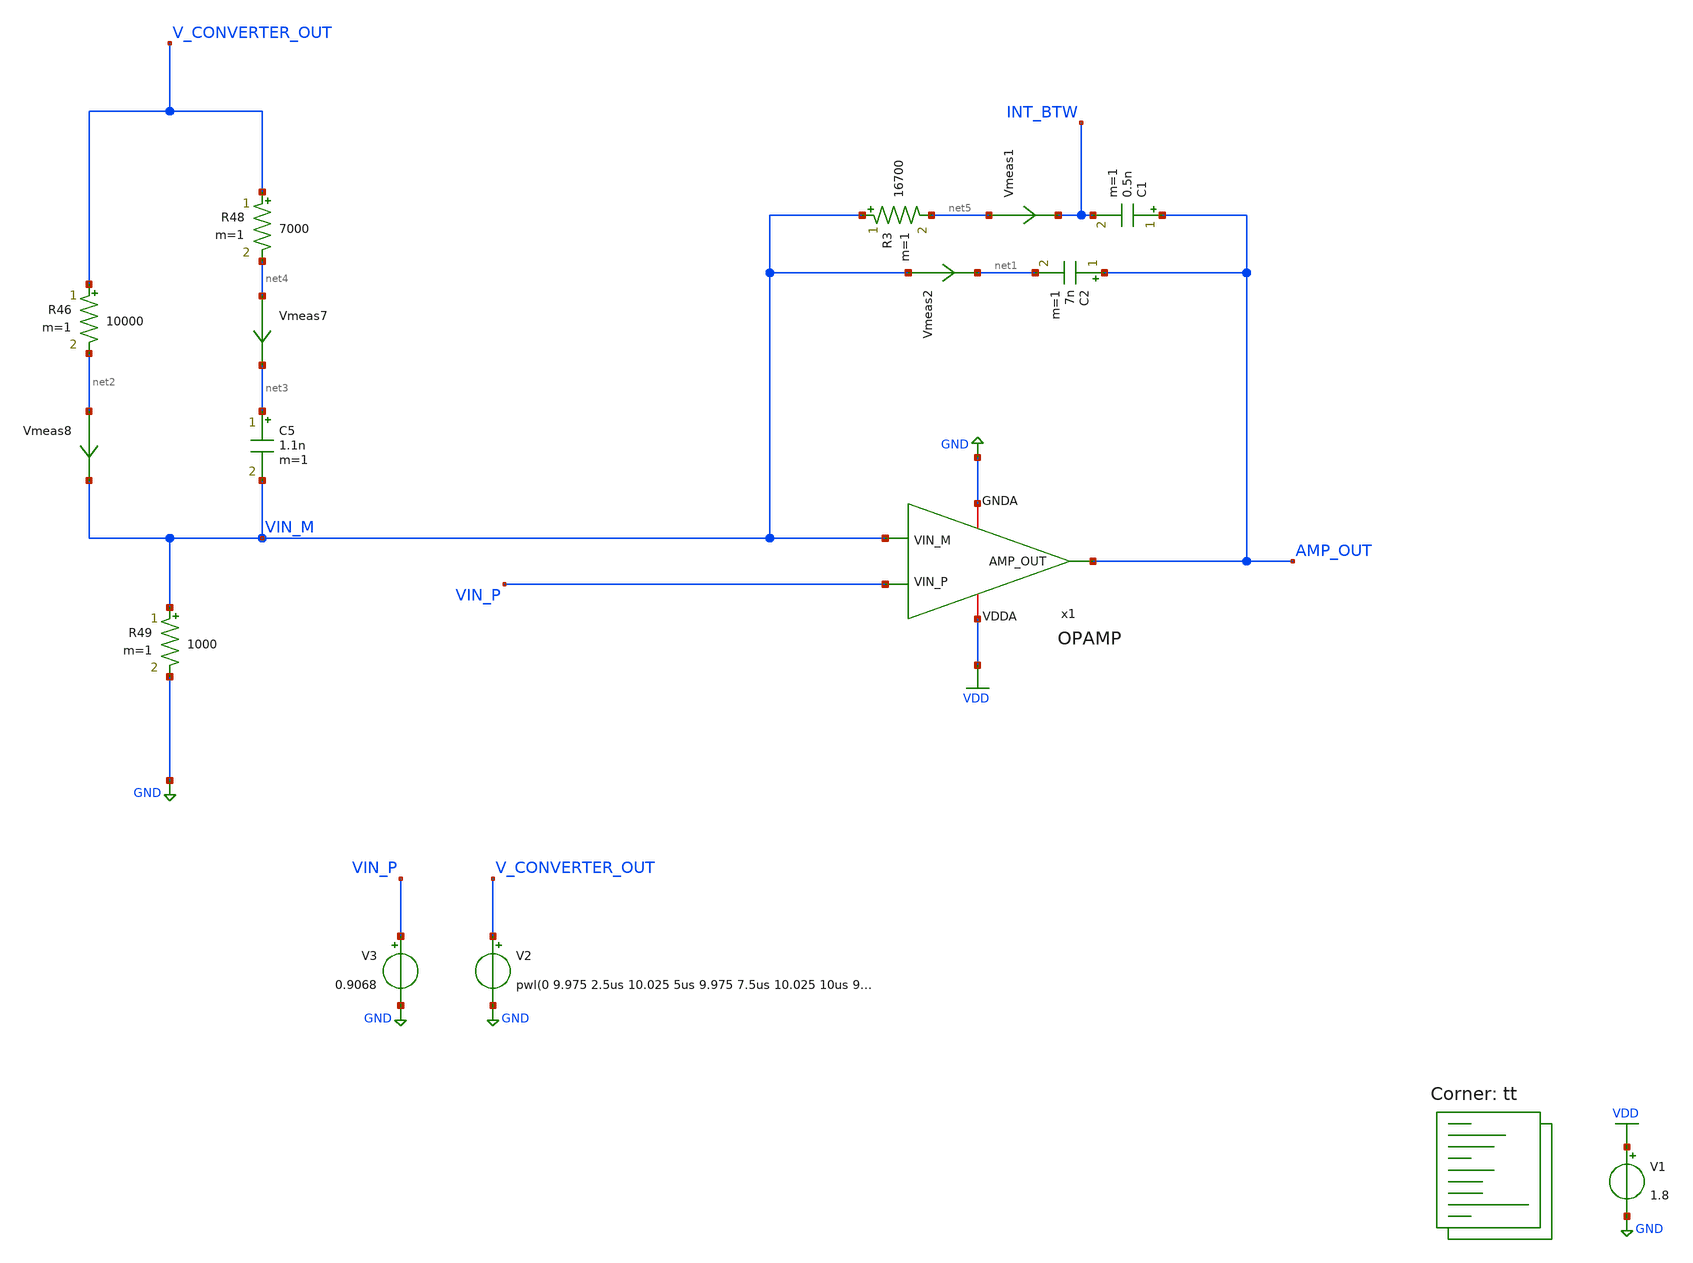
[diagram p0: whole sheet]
** sch_path: projects/ASU/EEE572/schematic/tb_integrator.sch
**.subckt tb_integrator
V1 VDD GND 1.8
V2 V_CONVERTER_OUT GND pwl(0 9.975 2.5us 10.025 5us 9.975 7.5us 10.025 10us 9.975 12.5us 10.025 15us
+ 9.975 17.5us 10.025 20us 9.975 22.5us 10.025 25us 9.975)
x1 VDD AMP_OUT VIN_P VIN_M GND OPAMP
V3 VIN_P GND 0.9068
C1 AMP_OUT INT_BTW 0.5n m=1
C2 AMP_OUT net1 7n m=1
Vmeas1 net5 INT_BTW 0
.save i(vmeas1)
Vmeas2 VIN_M net1 0
.save i(vmeas2)
R46 V_CONVERTER_OUT net2 10000 m=1
R48 V_CONVERTER_OUT net4 7000 m=1
C5 net3 VIN_M 1.1n m=1
R49 VIN_M GND 1000 m=1
Vmeas7 net4 net3 0
.save i(vmeas7)
Vmeas8 net2 VIN_M 0
.save i(vmeas8)
R3 VIN_M net5 16700 m=1
**** begin user architecture code
.lib $::SKYWATER_MODELS/sky130.lib.spice tt



.options method=gear
.options wnflag=1
* .options savecurrents

.control

  save v(vin_p) v(vin_m) v(vin_m2) v(int_btw) v(v_converter_out) v(amp_out) v(ph(amp_out))
  * save all
  * tran 0.1ns 4us
  * tran 0.01ns 0.4us
  tran 0.5ns 25us
  remzerovec
  write tb_integrator.raw
  set appendwrite

.endc




**** end user architecture code
**.ends

* expanding   symbol:  OPAMP.sym # of pins=5
** sym_path: projects/ASU/EEE572/schematic/OPAMP.sym
** sch_path: projects/ASU/EEE572/schematic/OPAMP.sch
.subckt OPAMP VDDA AMP_OUT VIN_P VIN_M GNDA
*.iopin GNDA
*.iopin VDDA
*.ipin VIN_P
*.ipin VIN_M
*.opin AMP_OUT
XM1 V_REF V_REF V_RES GNDA sky130_fd_pr__nfet_01v8 L=0.3 W=16 nf=8 ad='int((nf+1)/2) * W/nf * 0.29' as='int((nf+2)/2) * W/nf * 0.29'
+ pd='2*int((nf+1)/2) * (W/nf + 0.29)' ps='2*int((nf+2)/2) * (W/nf + 0.29)' nrd='0.29 / W' nrs='0.29 / W'
+ sa=0 sb=0 sd=0 mult=1 m=1
XM2 V_REF_MIR V_REF_MIR GNDA GNDA sky130_fd_pr__nfet_01v8 L=0.3 W=4 nf=2 ad='int((nf+1)/2) * W/nf * 0.29'
+ as='int((nf+2)/2) * W/nf * 0.29' pd='2*int((nf+1)/2) * (W/nf + 0.29)' ps='2*int((nf+2)/2) * (W/nf + 0.29)'
+ nrd='0.29 / W' nrs='0.29 / W' sa=0 sb=0 sd=0 mult=1 m=1
XM5 START_UP V_REF_MIR GNDA GNDA sky130_fd_pr__nfet_01v8 L=0.3 W=4 nf=2 ad='int((nf+1)/2) * W/nf * 0.29'
+ as='int((nf+2)/2) * W/nf * 0.29' pd='2*int((nf+1)/2) * (W/nf + 0.29)' ps='2*int((nf+2)/2) * (W/nf + 0.29)'
+ nrd='0.29 / W' nrs='0.29 / W' sa=0 sb=0 sd=0 mult=1 m=1
XM7 Vbiasp START_UP V_REF_MIR GNDA sky130_fd_pr__nfet_01v8 L=0.3 W=4 nf=2 ad='int((nf+1)/2) * W/nf * 0.29'
+ as='int((nf+2)/2) * W/nf * 0.29' pd='2*int((nf+1)/2) * (W/nf + 0.29)' ps='2*int((nf+2)/2) * (W/nf + 0.29)'
+ nrd='0.29 / W' nrs='0.29 / W' sa=0 sb=0 sd=0 mult=1 m=1
XM6 START_UP START_UP VDD VDD sky130_fd_pr__pfet_01v8 L=20 W=0.5 nf=1 ad='int((nf+1)/2) * W/nf * 0.29'
+ as='int((nf+2)/2) * W/nf * 0.29' pd='2*int((nf+1)/2) * (W/nf + 0.29)' ps='2*int((nf+2)/2) * (W/nf + 0.29)'
+ nrd='0.29 / W' nrs='0.29 / W' sa=0 sb=0 sd=0 mult=1 m=1
XM3 V_REF Vbiasp VDDA VDDA sky130_fd_pr__pfet_01v8 L=0.3 W=12 nf=6 ad='int((nf+1)/2) * W/nf * 0.29' as='int((nf+2)/2) * W/nf * 0.29'
+ pd='2*int((nf+1)/2) * (W/nf + 0.29)' ps='2*int((nf+2)/2) * (W/nf + 0.29)' nrd='0.29 / W' nrs='0.29 / W'
+ sa=0 sb=0 sd=0 mult=1 m=1
XM4 V_REF_MIR Vbiasp VDDA VDDA sky130_fd_pr__pfet_01v8 L=0.3 W=12 nf=6 ad='int((nf+1)/2) * W/nf * 0.29'
+ as='int((nf+2)/2) * W/nf * 0.29' pd='2*int((nf+1)/2) * (W/nf + 0.29)' ps='2*int((nf+2)/2) * (W/nf + 0.29)'
+ nrd='0.29 / W' nrs='0.29 / W' sa=0 sb=0 sd=0 mult=1 m=1
XM8 Vbiasp V_REF_MIR GNDA GNDA sky130_fd_pr__nfet_01v8 L=0.3 W=4 nf=2 ad='int((nf+1)/2) * W/nf * 0.29'
+ as='int((nf+2)/2) * W/nf * 0.29' pd='2*int((nf+1)/2) * (W/nf + 0.29)' ps='2*int((nf+2)/2) * (W/nf + 0.29)'
+ nrd='0.29 / W' nrs='0.29 / W' sa=0 sb=0 sd=0 mult=1 m=1
XM9 Vbiasp_MIR V_REF GNDA GNDA sky130_fd_pr__nfet_01v8 L=0.3 W=4 nf=2 ad='int((nf+1)/2) * W/nf * 0.29'
+ as='int((nf+2)/2) * W/nf * 0.29' pd='2*int((nf+1)/2) * (W/nf + 0.29)' ps='2*int((nf+2)/2) * (W/nf + 0.29)'
+ nrd='0.29 / W' nrs='0.29 / W' sa=0 sb=0 sd=0 mult=1 m=1
XM10 Vbiasp Vbiasp_MIR VDDA VDDA sky130_fd_pr__pfet_01v8 L=0.3 W=12 nf=6 ad='int((nf+1)/2) * W/nf * 0.29'
+ as='int((nf+2)/2) * W/nf * 0.29' pd='2*int((nf+1)/2) * (W/nf + 0.29)' ps='2*int((nf+2)/2) * (W/nf + 0.29)'
+ nrd='0.29 / W' nrs='0.29 / W' sa=0 sb=0 sd=0 mult=1 m=1
XM11 Vbiasp_MIR Vbiasp_MIR VDDA VDDA sky130_fd_pr__pfet_01v8 L=0.3 W=12 nf=6 ad='int((nf+1)/2) * W/nf * 0.29'
+ as='int((nf+2)/2) * W/nf * 0.29' pd='2*int((nf+1)/2) * (W/nf + 0.29)' ps='2*int((nf+2)/2) * (W/nf + 0.29)'
+ nrd='0.29 / W' nrs='0.29 / W' sa=0 sb=0 sd=0 mult=1 m=1
XM12 Vbias3 Vbias3 GNDA GNDA sky130_fd_pr__nfet_01v8 L=4 W=4 nf=1 ad='int((nf+1)/2) * W/nf * 0.29' as='int((nf+2)/2) * W/nf * 0.29'
+ pd='2*int((nf+1)/2) * (W/nf + 0.29)' ps='2*int((nf+2)/2) * (W/nf + 0.29)' nrd='0.29 / W' nrs='0.29 / W'
+ sa=0 sb=0 sd=0 mult=1 m=1
XM13 Vbias3 Vbiasp VDDA VDDA sky130_fd_pr__pfet_01v8 L=0.3 W=12 nf=6 ad='int((nf+1)/2) * W/nf * 0.29'
+ as='int((nf+2)/2) * W/nf * 0.29' pd='2*int((nf+1)/2) * (W/nf + 0.29)' ps='2*int((nf+2)/2) * (W/nf + 0.29)'
+ nrd='0.29 / W' nrs='0.29 / W' sa=0 sb=0 sd=0 mult=1 m=1
XM14 net1 Vbias1 VDDA VDDA sky130_fd_pr__pfet_01v8 L=0.3 W=12 nf=6 ad='int((nf+1)/2) * W/nf * 0.29' as='int((nf+2)/2) * W/nf * 0.29'
+ pd='2*int((nf+1)/2) * (W/nf + 0.29)' ps='2*int((nf+2)/2) * (W/nf + 0.29)' nrd='0.29 / W' nrs='0.29 / W'
+ sa=0 sb=0 sd=0 mult=1 m=1
XM15 Vhigh Vbias1 VDDA VDDA sky130_fd_pr__pfet_01v8 L=0.3 W=12 nf=6 ad='int((nf+1)/2) * W/nf * 0.29'
+ as='int((nf+2)/2) * W/nf * 0.29' pd='2*int((nf+1)/2) * (W/nf + 0.29)' ps='2*int((nf+2)/2) * (W/nf + 0.29)'
+ nrd='0.29 / W' nrs='0.29 / W' sa=0 sb=0 sd=0 mult=1 m=1
XM16 Vncas Vbias2 net1 VDDA sky130_fd_pr__pfet_01v8 L=0.3 W=12 nf=6 ad='int((nf+1)/2) * W/nf * 0.29'
+ as='int((nf+2)/2) * W/nf * 0.29' pd='2*int((nf+1)/2) * (W/nf + 0.29)' ps='2*int((nf+2)/2) * (W/nf + 0.29)'
+ nrd='0.29 / W' nrs='0.29 / W' sa=0 sb=0 sd=0 mult=1 m=1
XM17 Vbias1 Vbias2 Vhigh VDDA sky130_fd_pr__pfet_01v8 L=0.3 W=12 nf=6 ad='int((nf+1)/2) * W/nf * 0.29'
+ as='int((nf+2)/2) * W/nf * 0.29' pd='2*int((nf+1)/2) * (W/nf + 0.29)' ps='2*int((nf+2)/2) * (W/nf + 0.29)'
+ nrd='0.29 / W' nrs='0.29 / W' sa=0 sb=0 sd=0 mult=1 m=1
XM18 net2 Vbias4 GNDA GNDA sky130_fd_pr__nfet_01v8 L=0.3 W=4 nf=2 ad='int((nf+1)/2) * W/nf * 0.29' as='int((nf+2)/2) * W/nf * 0.29'
+ pd='2*int((nf+1)/2) * (W/nf + 0.29)' ps='2*int((nf+2)/2) * (W/nf + 0.29)' nrd='0.29 / W' nrs='0.29 / W'
+ sa=0 sb=0 sd=0 mult=1 m=1
XM19 Vncas Vncas Vncas_btw GNDA sky130_fd_pr__nfet_01v8 L=0.3 W=4 nf=2 ad='int((nf+1)/2) * W/nf * 0.29'
+ as='int((nf+2)/2) * W/nf * 0.29' pd='2*int((nf+1)/2) * (W/nf + 0.29)' ps='2*int((nf+2)/2) * (W/nf + 0.29)'
+ nrd='0.29 / W' nrs='0.29 / W' sa=0 sb=0 sd=0 mult=1 m=1
XM20 Vncas_btw Vbias3 net3 GNDA sky130_fd_pr__nfet_01v8 L=0.3 W=4 nf=2 ad='int((nf+1)/2) * W/nf * 0.29'
+ as='int((nf+2)/2) * W/nf * 0.29' pd='2*int((nf+1)/2) * (W/nf + 0.29)' ps='2*int((nf+2)/2) * (W/nf + 0.29)'
+ nrd='0.29 / W' nrs='0.29 / W' sa=0 sb=0 sd=0 mult=1 m=1
XM21 net3 Vncas_btw GNDA GNDA sky130_fd_pr__nfet_01v8 L=0.3 W=4 nf=2 ad='int((nf+1)/2) * W/nf * 0.29'
+ as='int((nf+2)/2) * W/nf * 0.29' pd='2*int((nf+1)/2) * (W/nf + 0.29)' ps='2*int((nf+2)/2) * (W/nf + 0.29)'
+ nrd='0.29 / W' nrs='0.29 / W' sa=0 sb=0 sd=0 mult=1 m=1
XM25 Vbias4 Vbiasp VDDA VDDA sky130_fd_pr__pfet_01v8 L=0.3 W=12 nf=6 ad='int((nf+1)/2) * W/nf * 0.29'
+ as='int((nf+2)/2) * W/nf * 0.29' pd='2*int((nf+1)/2) * (W/nf + 0.29)' ps='2*int((nf+2)/2) * (W/nf + 0.29)'
+ nrd='0.29 / W' nrs='0.29 / W' sa=0 sb=0 sd=0 mult=1 m=1
XM27 Vbias4 Vbias3 Vlow GNDA sky130_fd_pr__nfet_01v8 L=0.3 W=4 nf=2 ad='int((nf+1)/2) * W/nf * 0.29'
+ as='int((nf+2)/2) * W/nf * 0.29' pd='2*int((nf+1)/2) * (W/nf + 0.29)' ps='2*int((nf+2)/2) * (W/nf + 0.29)'
+ nrd='0.29 / W' nrs='0.29 / W' sa=0 sb=0 sd=0 mult=1 m=1
XM28 Vlow Vbias4 GNDA GNDA sky130_fd_pr__nfet_01v8 L=0.3 W=4 nf=2 ad='int((nf+1)/2) * W/nf * 0.29' as='int((nf+2)/2) * W/nf * 0.29'
+ pd='2*int((nf+1)/2) * (W/nf + 0.29)' ps='2*int((nf+2)/2) * (W/nf + 0.29)' nrd='0.29 / W' nrs='0.29 / W'
+ sa=0 sb=0 sd=0 mult=1 m=1
XM29 Vds2 Vgs2 VDDA VDDA sky130_fd_pr__pfet_01v8 L=0.15 W=12 nf=6 ad='int((nf+1)/2) * W/nf * 0.29' as='int((nf+2)/2) * W/nf * 0.29'
+ pd='2*int((nf+1)/2) * (W/nf + 0.29)' ps='2*int((nf+2)/2) * (W/nf + 0.29)' nrd='0.29 / W' nrs='0.29 / W'
+ sa=0 sb=0 sd=0 mult=1 m=1
XM30 Vgs2 Vbias2 Vds2 VDDA sky130_fd_pr__pfet_01v8 L=0.15 W=12 nf=6 ad='int((nf+1)/2) * W/nf * 0.29'
+ as='int((nf+2)/2) * W/nf * 0.29' pd='2*int((nf+1)/2) * (W/nf + 0.29)' ps='2*int((nf+2)/2) * (W/nf + 0.29)'
+ nrd='0.29 / W' nrs='0.29 / W' sa=0 sb=0 sd=0 mult=1 m=1
XM31 Vpcas Vbias3 Vds3 GNDA sky130_fd_pr__nfet_01v8 L=0.3 W=4 nf=2 ad='int((nf+1)/2) * W/nf * 0.29' as='int((nf+2)/2) * W/nf * 0.29'
+ pd='2*int((nf+1)/2) * (W/nf + 0.29)' ps='2*int((nf+2)/2) * (W/nf + 0.29)' nrd='0.29 / W' nrs='0.29 / W'
+ sa=0 sb=0 sd=0 mult=1 m=1
XM32 Vds3 Vbias4 GNDA GNDA sky130_fd_pr__nfet_01v8 L=0.3 W=4 nf=2 ad='int((nf+1)/2) * W/nf * 0.29' as='int((nf+2)/2) * W/nf * 0.29'
+ pd='2*int((nf+1)/2) * (W/nf + 0.29)' ps='2*int((nf+2)/2) * (W/nf + 0.29)' nrd='0.29 / W' nrs='0.29 / W'
+ sa=0 sb=0 sd=0 mult=1 m=1
XM33 Vpcas Vpcas Vgs2 VDDA sky130_fd_pr__pfet_01v8 L=0.15 W=12 nf=1 ad='int((nf+1)/2) * W/nf * 0.29'
+ as='int((nf+2)/2) * W/nf * 0.29' pd='2*int((nf+1)/2) * (W/nf + 0.29)' ps='2*int((nf+2)/2) * (W/nf + 0.29)'
+ nrd='0.29 / W' nrs='0.29 / W' sa=0 sb=0 sd=0 mult=1 m=1
XM22 Vbias1 Vbias3 net2 GNDA sky130_fd_pr__nfet_01v8 L=0.3 W=4 nf=2 ad='int((nf+1)/2) * W/nf * 0.29'
+ as='int((nf+2)/2) * W/nf * 0.29' pd='2*int((nf+1)/2) * (W/nf + 0.29)' ps='2*int((nf+2)/2) * (W/nf + 0.29)'
+ nrd='0.29 / W' nrs='0.29 / W' sa=0 sb=0 sd=0 mult=1 m=1
XM23 Vbias2 Vbias2 VDDA VDDA sky130_fd_pr__pfet_01v8 L=1.5 W=12 nf=1 ad='int((nf+1)/2) * W/nf * 0.29'
+ as='int((nf+2)/2) * W/nf * 0.29' pd='2*int((nf+1)/2) * (W/nf + 0.29)' ps='2*int((nf+2)/2) * (W/nf + 0.29)'
+ nrd='0.29 / W' nrs='0.29 / W' sa=0 sb=0 sd=0 mult=1 m=1
XM24 net4 Vbias4 GNDA GNDA sky130_fd_pr__nfet_01v8 L=0.3 W=4 nf=2 ad='int((nf+1)/2) * W/nf * 0.29' as='int((nf+2)/2) * W/nf * 0.29'
+ pd='2*int((nf+1)/2) * (W/nf + 0.29)' ps='2*int((nf+2)/2) * (W/nf + 0.29)' nrd='0.29 / W' nrs='0.29 / W'
+ sa=0 sb=0 sd=0 mult=1 m=1
XM26 Vbias2 Vbias3 net4 GNDA sky130_fd_pr__nfet_01v8 L=0.3 W=4 nf=2 ad='int((nf+1)/2) * W/nf * 0.29'
+ as='int((nf+2)/2) * W/nf * 0.29' pd='2*int((nf+1)/2) * (W/nf + 0.29)' ps='2*int((nf+2)/2) * (W/nf + 0.29)'
+ nrd='0.29 / W' nrs='0.29 / W' sa=0 sb=0 sd=0 mult=1 m=1
XC1 Vbiasp VDDA sky130_fd_pr__cap_mim_m3_1 W=2 L=2 MF=4 m=4
XR1 GNDA V_RES GNDA sky130_fd_pr__res_high_po_0p35 L=10 mult=1 m=1
XM34 V_tail_btw Vbias4 GNDA GNDA sky130_fd_pr__nfet_01v8 L=0.3 W=12 nf=4 ad='int((nf+1)/2) * W/nf * 0.29'
+ as='int((nf+2)/2) * W/nf * 0.29' pd='2*int((nf+1)/2) * (W/nf + 0.29)' ps='2*int((nf+2)/2) * (W/nf + 0.29)'
+ nrd='0.29 / W' nrs='0.29 / W' sa=0 sb=0 sd=0 mult=3 m=3
XM35 Vp Vbias3 V_tail_btw GNDA sky130_fd_pr__nfet_01v8 L=0.3 W=12 nf=4 ad='int((nf+1)/2) * W/nf * 0.29'
+ as='int((nf+2)/2) * W/nf * 0.29' pd='2*int((nf+1)/2) * (W/nf + 0.29)' ps='2*int((nf+2)/2) * (W/nf + 0.29)'
+ nrd='0.29 / W' nrs='0.29 / W' sa=0 sb=0 sd=0 mult=3 m=3
XM36 Vd1 VIN_P Vp GNDA sky130_fd_pr__nfet_01v8 L=0.3 W=12 nf=4 ad='int((nf+1)/2) * W/nf * 0.29' as='int((nf+2)/2) * W/nf * 0.29'
+ pd='2*int((nf+1)/2) * (W/nf + 0.29)' ps='2*int((nf+2)/2) * (W/nf + 0.29)' nrd='0.29 / W' nrs='0.29 / W'
+ sa=0 sb=0 sd=0 mult=2 m=2
XM37 Vd2 VIN_M Vp GNDA sky130_fd_pr__nfet_01v8 L=0.3 W=12 nf=4 ad='int((nf+1)/2) * W/nf * 0.29' as='int((nf+2)/2) * W/nf * 0.29'
+ pd='2*int((nf+1)/2) * (W/nf + 0.29)' ps='2*int((nf+2)/2) * (W/nf + 0.29)' nrd='0.29 / W' nrs='0.29 / W'
+ sa=0 sb=0 sd=0 mult=2 m=2
XM38 AMP_MIR Vb1 Vd1 GNDA sky130_fd_pr__nfet_01v8 L=0.3 W=12 nf=4 ad='int((nf+1)/2) * W/nf * 0.29' as='int((nf+2)/2) * W/nf * 0.29'
+ pd='2*int((nf+1)/2) * (W/nf + 0.29)' ps='2*int((nf+2)/2) * (W/nf + 0.29)' nrd='0.29 / W' nrs='0.29 / W'
+ sa=0 sb=0 sd=0 mult=2 m=2
XM39 AMP_OUT Vb1 Vd2 GNDA sky130_fd_pr__nfet_01v8 L=0.3 W=12 nf=4 ad='int((nf+1)/2) * W/nf * 0.29' as='int((nf+2)/2) * W/nf * 0.29'
+ pd='2*int((nf+1)/2) * (W/nf + 0.29)' ps='2*int((nf+2)/2) * (W/nf + 0.29)' nrd='0.29 / W' nrs='0.29 / W'
+ sa=0 sb=0 sd=0 mult=2 m=2
XM40 net6 AMP_MIR VDDA VDDA sky130_fd_pr__pfet_01v8 L=0.3 W=12 nf=4 ad='int((nf+1)/2) * W/nf * 0.29'
+ as='int((nf+2)/2) * W/nf * 0.29' pd='2*int((nf+1)/2) * (W/nf + 0.29)' ps='2*int((nf+2)/2) * (W/nf + 0.29)'
+ nrd='0.29 / W' nrs='0.29 / W' sa=0 sb=0 sd=0 mult=6 m=6
XM41 net5 AMP_MIR VDDA VDDA sky130_fd_pr__pfet_01v8 L=0.3 W=12 nf=4 ad='int((nf+1)/2) * W/nf * 0.29'
+ as='int((nf+2)/2) * W/nf * 0.29' pd='2*int((nf+1)/2) * (W/nf + 0.29)' ps='2*int((nf+2)/2) * (W/nf + 0.29)'
+ nrd='0.29 / W' nrs='0.29 / W' sa=0 sb=0 sd=0 mult=6 m=6
XM42 AMP_OUT Vbias2 net6 VDDA sky130_fd_pr__pfet_01v8 L=0.3 W=12 nf=4 ad='int((nf+1)/2) * W/nf * 0.29'
+ as='int((nf+2)/2) * W/nf * 0.29' pd='2*int((nf+1)/2) * (W/nf + 0.29)' ps='2*int((nf+2)/2) * (W/nf + 0.29)'
+ nrd='0.29 / W' nrs='0.29 / W' sa=0 sb=0 sd=0 mult=6 m=6
XM43 AMP_MIR Vbias2 net5 VDDA sky130_fd_pr__pfet_01v8 L=0.3 W=12 nf=4 ad='int((nf+1)/2) * W/nf * 0.29'
+ as='int((nf+2)/2) * W/nf * 0.29' pd='2*int((nf+1)/2) * (W/nf + 0.29)' ps='2*int((nf+2)/2) * (W/nf + 0.29)'
+ nrd='0.29 / W' nrs='0.29 / W' sa=0 sb=0 sd=0 mult=6 m=6
XM44 Vb1 Vb1 Vp GNDA sky130_fd_pr__nfet_01v8 L=1 W=1 nf=1 ad='int((nf+1)/2) * W/nf * 0.29' as='int((nf+2)/2) * W/nf * 0.29'
+ pd='2*int((nf+1)/2) * (W/nf + 0.29)' ps='2*int((nf+2)/2) * (W/nf + 0.29)' nrd='0.29 / W' nrs='0.29 / W'
+ sa=0 sb=0 sd=0 mult=1 m=1
XM45 net7 Vbias1 VDDA VDDA sky130_fd_pr__pfet_01v8 L=0.3 W=12 nf=4 ad='int((nf+1)/2) * W/nf * 0.29' as='int((nf+2)/2) * W/nf * 0.29'
+ pd='2*int((nf+1)/2) * (W/nf + 0.29)' ps='2*int((nf+2)/2) * (W/nf + 0.29)' nrd='0.29 / W' nrs='0.29 / W'
+ sa=0 sb=0 sd=0 mult=1 m=1
XM46 Vb1 Vbias2 net7 VDDA sky130_fd_pr__pfet_01v8 L=0.3 W=12 nf=4 ad='int((nf+1)/2) * W/nf * 0.29' as='int((nf+2)/2) * W/nf * 0.29'
+ pd='2*int((nf+1)/2) * (W/nf + 0.29)' ps='2*int((nf+2)/2) * (W/nf + 0.29)' nrd='0.29 / W' nrs='0.29 / W'
+ sa=0 sb=0 sd=0 mult=1 m=1
.ends

.GLOBAL GND
.GLOBAL VDD
.end
